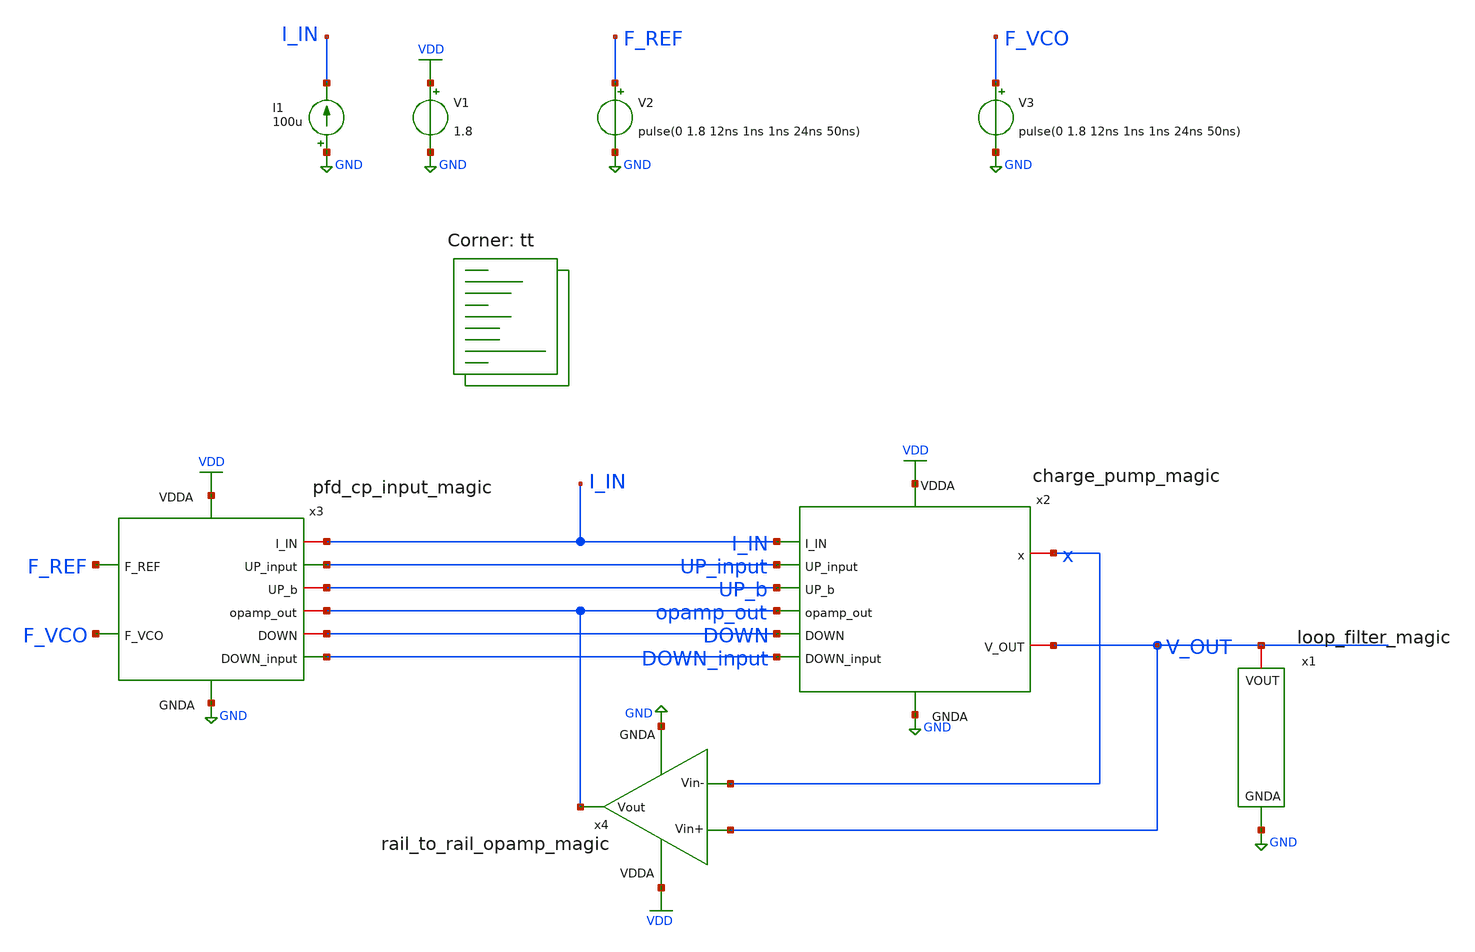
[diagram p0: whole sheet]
** sch_path: projects/pll/charge_pump/magic/pfd_charge_pump_magic_2.sch
**.subckt pfd_charge_pump_magic_2
V1 VDD GND 1.8
V2 F_REF GND pulse(0 1.8 12ns 1ns 1ns 24ns 50ns)
V3 F_VCO GND pulse(0 1.8 12ns 1ns 1ns 24ns 50ns)
I1 GND I_IN 100u
x3 DOWN_input VDD GND UP_input net1 F_REF I_IN F_VCO UP_b DOWN pfd_cp_input_magic
x2 VDD GND x V_OUT UP_b DOWN I_IN UP_input DOWN_input opamp_out charge_pump_magic
x4 VDD V_OUT x opamp_out GND rail_to_rail_opamp_magic
x1 V_OUT GND loop_filter_magic
**** begin user architecture code
.lib $::SKYWATER_MODELS/sky130.lib.spice tt



.include /foss/designs/my_design/projects/pll/charge_pump/magic/pfd_cp_input_magic.spice
.include /foss/designs/my_design/projects/pll/charge_pump/magic/charge_pump_magic.spice
.include /foss/designs/my_design/projects/pll/charge_pump/magic/rail_to_rail_opamp_magic.spice
.include /foss/designs/my_design/projects/pll/charge_pump/magic/loop_filter_magic.spice

.option method=gear
.option wnflag=1
.option savecurrents

* V_out initial voltage value for the F_VCO delay of 2ns  (leading)
* .ic v(v_out) = 1.8

* V_out initial voltage value for the F_VCO delay of 12ns (lock condition)
.ic v(v_out) = 0.9

* V_out initial voltage value for the F_VCO delay of 22ns (lagging)
* .ic v(v_out) = 0.0

.control
  save v(f_ref) save v(f_vco) save v(i_in) save v(up_pfd) v(down_pfd) v(up_pfd_b) v(down_pfd_b)
+ v(up) v(up_b) v(down) v(down_b) v(x) v(opamp_out) v(up_input) v(down_input) v(down_gate) v(v_out)
  * save all

  * timestep for exact simulation results
  * tran 5ps 0.5us

  * timestep for faster simulation results
  tran 50ps 0.5us

  remzerovec
  write pfd_charge_pump_magic_2.raw
  set appendwrite

.endc



**** end user architecture code
**.ends
.GLOBAL GND
.GLOBAL VDD
.end
